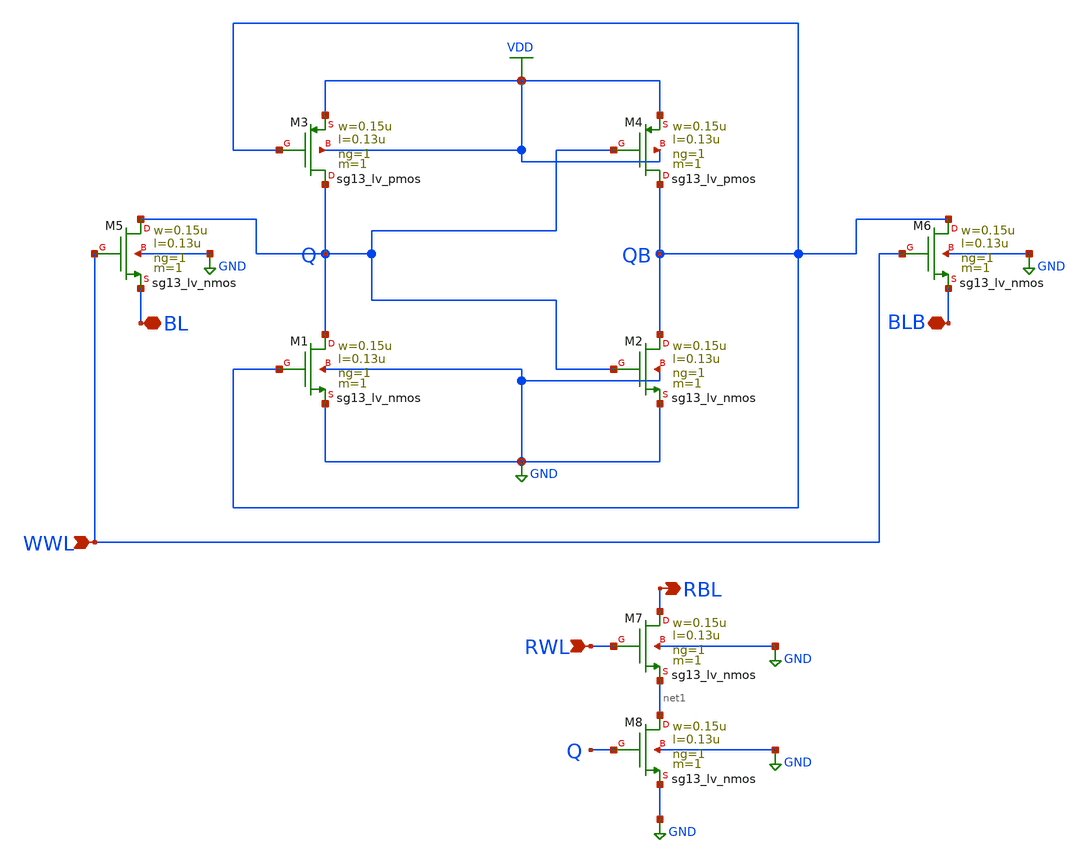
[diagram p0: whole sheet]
** sch_path: sram8t/schematic/sram8t.sch
**.subckt sram8t BL BLB WWL RWL RBL
*.iopin BL
*.iopin BLB
*.ipin WWL
*.ipin RWL
*.opin RBL
XM1 Q QB GND GND sg13_lv_nmos w=0.15u l=0.13u ng=1 m=1 mm_ok=1
XM2 QB Q GND GND sg13_lv_nmos w=0.15u l=0.13u ng=1 m=1 mm_ok=1
XM3 Q QB VDD VDD sg13_lv_pmos w=0.15u l=0.13u ng=1 m=1 mm_ok=1
XM4 QB Q VDD VDD sg13_lv_pmos w=0.15u l=0.13u ng=1 m=1 mm_ok=1
XM5 Q WWL BL GND sg13_lv_nmos w=0.15u l=0.13u ng=1 m=1 mm_ok=1
XM6 QB WWL BLB GND sg13_lv_nmos w=0.15u l=0.13u ng=1 m=1 mm_ok=1
XM7 RBL RWL net1 GND sg13_lv_nmos w=0.15u l=0.13u ng=1 m=1 mm_ok=1
XM8 net1 Q GND GND sg13_lv_nmos w=0.15u l=0.13u ng=1 m=1 mm_ok=1
**.ends
.GLOBAL GND
.GLOBAL VDD
.end
